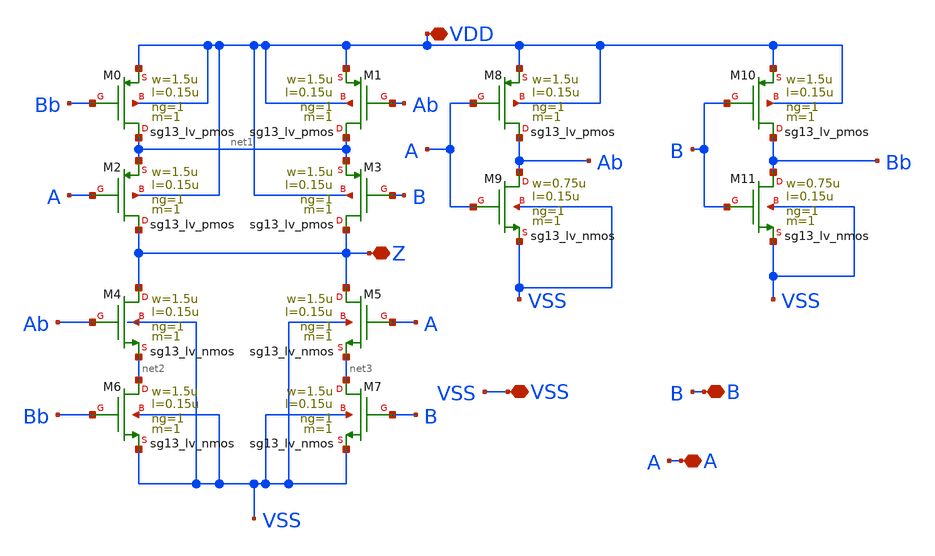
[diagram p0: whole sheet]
** sch_path: design/blocks/xorgate/schematic/XORGATE.sch
**.subckt XORGATE Z B VDD A VSS
*.iopin Z
*.iopin B
*.iopin VDD
*.iopin A
*.iopin VSS
XM1 net1 Ab VDD VDD sg13_lv_pmos w=1.5u l=0.15u ng=1 m=1 mm_ok=1
XM4 Z Ab net2 VSS sg13_lv_nmos w=1.5u l=0.15u ng=1 m=1 mm_ok=1
XM0 net1 Bb VDD VDD sg13_lv_pmos w=1.5u l=0.15u ng=1 m=1 mm_ok=1
XM3 Z B net1 VDD sg13_lv_pmos w=1.5u l=0.15u ng=1 m=1 mm_ok=1
XM2 Z A net1 VDD sg13_lv_pmos w=1.5u l=0.15u ng=1 m=1 mm_ok=1
XM8 Ab A VDD VDD sg13_lv_pmos w=1.5u l=0.15u ng=1 m=1 mm_ok=1
XM10 Bb B VDD VDD sg13_lv_pmos w=1.5u l=0.15u ng=1 m=1 mm_ok=1
XM5 Z A net3 VSS sg13_lv_nmos w=1.5u l=0.15u ng=1 m=1 mm_ok=1
XM9 Ab A VSS VSS sg13_lv_nmos w=0.75u l=0.15u ng=1 m=1 mm_ok=1
XM6 net2 Bb VSS VSS sg13_lv_nmos w=1.5u l=0.15u ng=1 m=1 mm_ok=1
XM11 Bb B VSS VSS sg13_lv_nmos w=0.75u l=0.15u ng=1 m=1 mm_ok=1
XM7 net3 B VSS VSS sg13_lv_nmos w=1.5u l=0.15u ng=1 m=1 mm_ok=1
**.ends
.end
